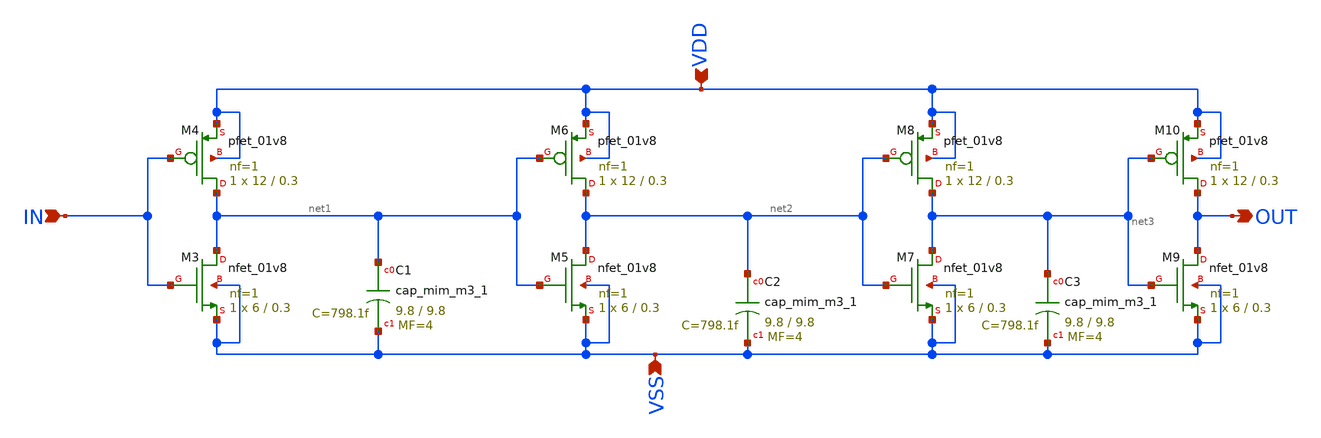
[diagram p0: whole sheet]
** sch_path: Delay_cell.sch
**.subckt Delay_cell IN VSS VDD OUT
*.ipin IN
*.ipin VSS
*.ipin VDD
*.opin OUT
XM3 net1 IN VSS VSS sky130_fd_pr__nfet_01v8 L=0.3 W=6 nf=1 ad='int((nf+1)/2) * W/nf * 0.29' as='int((nf+2)/2) * W/nf * 0.29'
+ pd='2*int((nf+1)/2) * (W/nf + 0.29)' ps='2*int((nf+2)/2) * (W/nf + 0.29)' nrd='0.29 / W' nrs='0.29 / W'
+ sa=0 sb=0 sd=0 mult=1 m=1
XM4 net1 IN VDD VDD sky130_fd_pr__pfet_01v8 L=0.3 W=12 nf=1 ad='int((nf+1)/2) * W/nf * 0.29' as='int((nf+2)/2) * W/nf * 0.29'
+ pd='2*int((nf+1)/2) * (W/nf + 0.29)' ps='2*int((nf+2)/2) * (W/nf + 0.29)' nrd='0.29 / W' nrs='0.29 / W'
+ sa=0 sb=0 sd=0 mult=1 m=1
XM5 net2 net1 VSS VSS sky130_fd_pr__nfet_01v8 L=0.3 W=6 nf=1 ad='int((nf+1)/2) * W/nf * 0.29' as='int((nf+2)/2) * W/nf * 0.29'
+ pd='2*int((nf+1)/2) * (W/nf + 0.29)' ps='2*int((nf+2)/2) * (W/nf + 0.29)' nrd='0.29 / W' nrs='0.29 / W'
+ sa=0 sb=0 sd=0 mult=1 m=1
XM6 net2 net1 VDD VDD sky130_fd_pr__pfet_01v8 L=0.3 W=12 nf=1 ad='int((nf+1)/2) * W/nf * 0.29' as='int((nf+2)/2) * W/nf * 0.29'
+ pd='2*int((nf+1)/2) * (W/nf + 0.29)' ps='2*int((nf+2)/2) * (W/nf + 0.29)' nrd='0.29 / W' nrs='0.29 / W'
+ sa=0 sb=0 sd=0 mult=1 m=1
XM7 net3 net2 VSS VSS sky130_fd_pr__nfet_01v8 L=0.3 W=6 nf=1 ad='int((nf+1)/2) * W/nf * 0.29' as='int((nf+2)/2) * W/nf * 0.29'
+ pd='2*int((nf+1)/2) * (W/nf + 0.29)' ps='2*int((nf+2)/2) * (W/nf + 0.29)' nrd='0.29 / W' nrs='0.29 / W'
+ sa=0 sb=0 sd=0 mult=1 m=1
XM8 net3 net2 VDD VDD sky130_fd_pr__pfet_01v8 L=0.3 W=12 nf=1 ad='int((nf+1)/2) * W/nf * 0.29' as='int((nf+2)/2) * W/nf * 0.29'
+ pd='2*int((nf+1)/2) * (W/nf + 0.29)' ps='2*int((nf+2)/2) * (W/nf + 0.29)' nrd='0.29 / W' nrs='0.29 / W'
+ sa=0 sb=0 sd=0 mult=1 m=1
XM9 OUT net3 VSS VSS sky130_fd_pr__nfet_01v8 L=0.3 W=6 nf=1 ad='int((nf+1)/2) * W/nf * 0.29' as='int((nf+2)/2) * W/nf * 0.29'
+ pd='2*int((nf+1)/2) * (W/nf + 0.29)' ps='2*int((nf+2)/2) * (W/nf + 0.29)' nrd='0.29 / W' nrs='0.29 / W'
+ sa=0 sb=0 sd=0 mult=1 m=1
XM10 OUT net3 VDD VDD sky130_fd_pr__pfet_01v8 L=0.3 W=12 nf=1 ad='int((nf+1)/2) * W/nf * 0.29' as='int((nf+2)/2) * W/nf * 0.29'
+ pd='2*int((nf+1)/2) * (W/nf + 0.29)' ps='2*int((nf+2)/2) * (W/nf + 0.29)' nrd='0.29 / W' nrs='0.29 / W'
+ sa=0 sb=0 sd=0 mult=1 m=1
XC1 net1 VSS sky130_fd_pr__cap_mim_m3_1 W=9.8 L=9.8 MF=4 m=4
XC2 net2 VSS sky130_fd_pr__cap_mim_m3_1 W=9.8 L=9.8 MF=4 m=4
XC3 net3 VSS sky130_fd_pr__cap_mim_m3_1 W=9.8 L=9.8 MF=4 m=4
**.ends
.end
